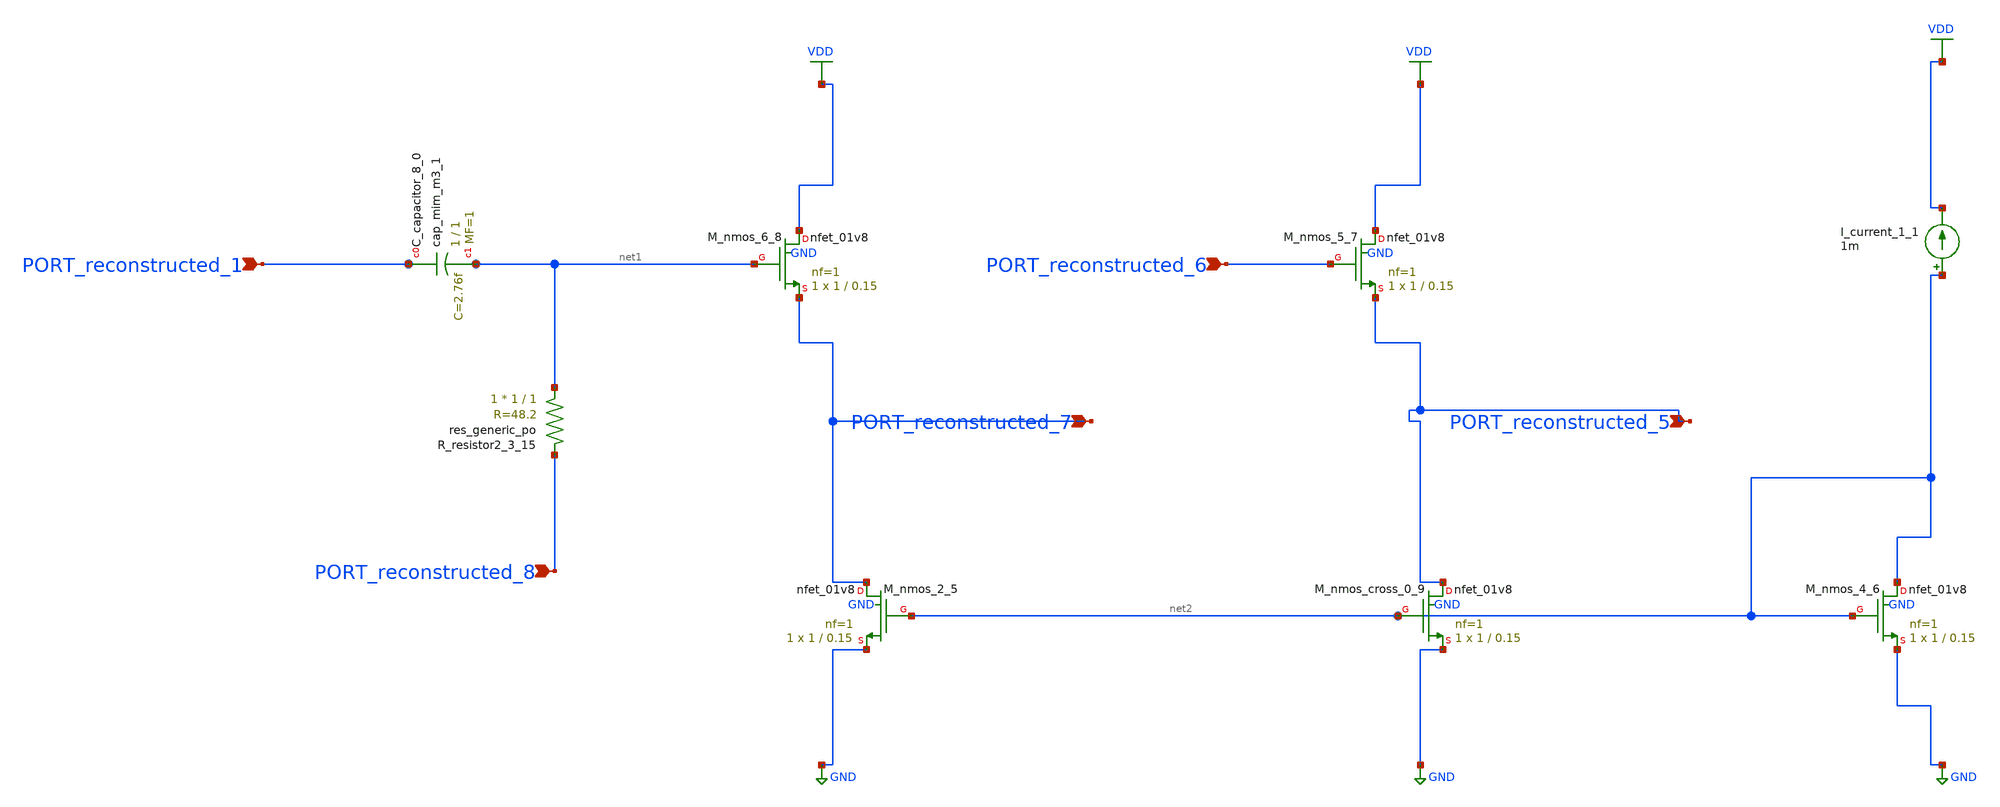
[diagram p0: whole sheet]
** sch_path: schematics/SchemGen/10_1016_j_aeue_2023_154777_04_002.sch
**.subckt 10_1016_j_aeue_2023_154777_04_002 PORT_reconstructed_6 PORT_reconstructed_7
*+ PORT_reconstructed_1 PORT_reconstructed_5 PORT_reconstructed_8
*.ipin PORT_reconstructed_6
*.ipin PORT_reconstructed_7
*.ipin PORT_reconstructed_1
*.ipin PORT_reconstructed_5
*.ipin PORT_reconstructed_8
XC_capacitor_8_0 PORT_reconstructed_1 net1 sky130_fd_pr__cap_mim_m3_1 W=1 L=1 MF=1 m=1
I_current_1_1 net2 VDD 1m
XM_nmos_2_5 PORT_reconstructed_7 net2 GND GND sky130_fd_pr__nfet_01v8 L=0.15 W=1 nf=1 ad='int((1 + 1)/2) * 1 / 1 * 0.29'
+ as='int((1 + 2)/2) * 1 / 1 * 0.29' pd='2*int((1 + 1)/2) * (1 / 1 + 0.29)' ps='2*int((1 + 2)/2) * (1 / 1 + 0.29)'
+ nrd='0.29 / 1 ' nrs='0.29 / 1 ' sa=0 sb=0 sd=0 mult=1 m=1
XM_nmos_4_6 net2 net2 GND GND sky130_fd_pr__nfet_01v8 L=0.15 W=1 nf=1 ad='int((1 + 1)/2) * 1 / 1 * 0.29'
+ as='int((1 + 2)/2) * 1 / 1 * 0.29' pd='2*int((1 + 1)/2) * (1 / 1 + 0.29)' ps='2*int((1 + 2)/2) * (1 / 1 + 0.29)'
+ nrd='0.29 / 1 ' nrs='0.29 / 1 ' sa=0 sb=0 sd=0 mult=1 m=1
XM_nmos_5_7 VDD PORT_reconstructed_6 PORT_reconstructed_5 GND sky130_fd_pr__nfet_01v8 L=0.15 W=1 nf=1
+ ad='int((1 + 1)/2) * 1 / 1 * 0.29' as='int((1 + 2)/2) * 1 / 1 * 0.29' pd='2*int((1 + 1)/2) * (1 / 1 + 0.29)'
+ ps='2*int((1 + 2)/2) * (1 / 1 + 0.29)' nrd='0.29 / 1 ' nrs='0.29 / 1 ' sa=0 sb=0 sd=0 mult=1 m=1
XM_nmos_6_8 VDD net1 PORT_reconstructed_7 GND sky130_fd_pr__nfet_01v8 L=0.15 W=1 nf=1 ad='int((1 + 1)/2) * 1 / 1 * 0.29'
+ as='int((1 + 2)/2) * 1 / 1 * 0.29' pd='2*int((1 + 1)/2) * (1 / 1 + 0.29)' ps='2*int((1 + 2)/2) * (1 / 1 + 0.29)'
+ nrd='0.29 / 1 ' nrs='0.29 / 1 ' sa=0 sb=0 sd=0 mult=1 m=1
XM_nmos_cross_0_9 PORT_reconstructed_5 net2 GND GND sky130_fd_pr__nfet_01v8 L=0.15 W=1 nf=1 ad='int((1 + 1)/2) * 1 / 1 * 0.29'
+ as='int((1 + 2)/2) * 1 / 1 * 0.29' pd='2*int((1 + 1)/2) * (1 / 1 + 0.29)' ps='2*int((1 + 2)/2) * (1 / 1 + 0.29)'
+ nrd='0.29 / 1 ' nrs='0.29 / 1 ' sa=0 sb=0 sd=0 mult=1 m=1
XR_resistor2_3_15 net1 PORT_reconstructed_8 sky130_fd_pr__res_generic_po W=1 L=1 m=1
**.ends
.GLOBAL GND
.GLOBAL VDD
.end
